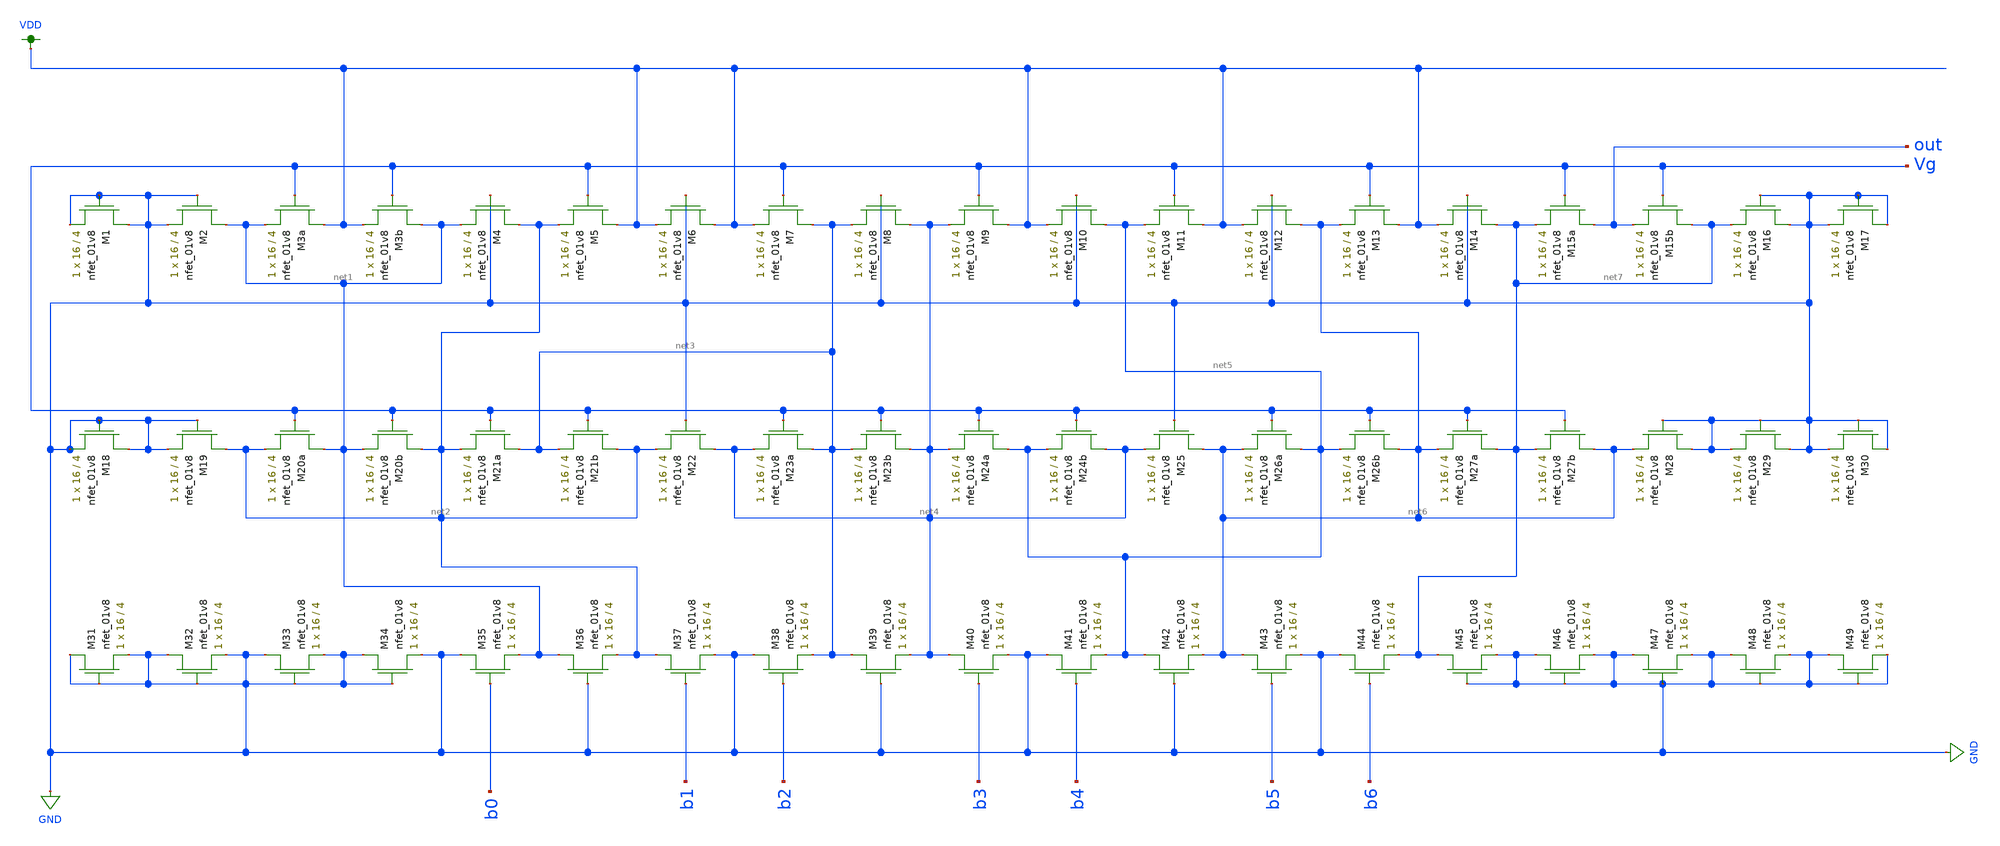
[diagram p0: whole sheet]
** sch_path: schematic/LDS/dac_7_bit_LDS.sch
**.subckt dac_7_bit_LDS
XM3a VDD Vg net1 GND sky130_fd_pr__nfet_01v8 L=4 W=16 nf=1 ad='int((nf+1)/2) * W/nf * 0.29' as='int((nf+2)/2) * W/nf * 0.29'
+ pd='2*int((nf+1)/2) * (W/nf + 0.29)' ps='2*int((nf+2)/2) * (W/nf + 0.29)' nrd='0.29 / W' nrs='0.29 / W'
+ sa=0 sb=0 sd=0 mult=1 m=1
XM3b net1 Vg VDD GND sky130_fd_pr__nfet_01v8 L=4 W=16 nf=1 ad='int((nf+1)/2) * W/nf * 0.29' as='int((nf+2)/2) * W/nf * 0.29'
+ pd='2*int((nf+1)/2) * (W/nf + 0.29)' ps='2*int((nf+2)/2) * (W/nf + 0.29)' nrd='0.29 / W' nrs='0.29 / W'
+ sa=0 sb=0 sd=0 mult=1 m=1
XM4 net2 GND net1 GND sky130_fd_pr__nfet_01v8 L=4 W=16 nf=1 ad='int((nf+1)/2) * W/nf * 0.29' as='int((nf+2)/2) * W/nf * 0.29'
+ pd='2*int((nf+1)/2) * (W/nf + 0.29)' ps='2*int((nf+2)/2) * (W/nf + 0.29)' nrd='0.29 / W' nrs='0.29 / W'
+ sa=0 sb=0 sd=0 mult=1 m=1
XM5 VDD Vg net2 GND sky130_fd_pr__nfet_01v8 L=4 W=16 nf=1 ad='int((nf+1)/2) * W/nf * 0.29' as='int((nf+2)/2) * W/nf * 0.29'
+ pd='2*int((nf+1)/2) * (W/nf + 0.29)' ps='2*int((nf+2)/2) * (W/nf + 0.29)' nrd='0.29 / W' nrs='0.29 / W'
+ sa=0 sb=0 sd=0 mult=1 m=1
XM6 VDD GND VDD GND sky130_fd_pr__nfet_01v8 L=4 W=16 nf=1 ad='int((nf+1)/2) * W/nf * 0.29' as='int((nf+2)/2) * W/nf * 0.29'
+ pd='2*int((nf+1)/2) * (W/nf + 0.29)' ps='2*int((nf+2)/2) * (W/nf + 0.29)' nrd='0.29 / W' nrs='0.29 / W'
+ sa=0 sb=0 sd=0 mult=1 m=1
XM7 net3 Vg VDD GND sky130_fd_pr__nfet_01v8 L=4 W=16 nf=1 ad='int((nf+1)/2) * W/nf * 0.29' as='int((nf+2)/2) * W/nf * 0.29'
+ pd='2*int((nf+1)/2) * (W/nf + 0.29)' ps='2*int((nf+2)/2) * (W/nf + 0.29)' nrd='0.29 / W' nrs='0.29 / W'
+ sa=0 sb=0 sd=0 mult=1 m=1
XM8 net4 GND net3 GND sky130_fd_pr__nfet_01v8 L=4 W=16 nf=1 ad='int((nf+1)/2) * W/nf * 0.29' as='int((nf+2)/2) * W/nf * 0.29'
+ pd='2*int((nf+1)/2) * (W/nf + 0.29)' ps='2*int((nf+2)/2) * (W/nf + 0.29)' nrd='0.29 / W' nrs='0.29 / W'
+ sa=0 sb=0 sd=0 mult=1 m=1
XM9 VDD Vg net4 GND sky130_fd_pr__nfet_01v8 L=4 W=16 nf=1 ad='int((nf+1)/2) * W/nf * 0.29' as='int((nf+2)/2) * W/nf * 0.29'
+ pd='2*int((nf+1)/2) * (W/nf + 0.29)' ps='2*int((nf+2)/2) * (W/nf + 0.29)' nrd='0.29 / W' nrs='0.29 / W'
+ sa=0 sb=0 sd=0 mult=1 m=1
XM10 net5 GND VDD GND sky130_fd_pr__nfet_01v8 L=4 W=16 nf=1 ad='int((nf+1)/2) * W/nf * 0.29' as='int((nf+2)/2) * W/nf * 0.29'
+ pd='2*int((nf+1)/2) * (W/nf + 0.29)' ps='2*int((nf+2)/2) * (W/nf + 0.29)' nrd='0.29 / W' nrs='0.29 / W'
+ sa=0 sb=0 sd=0 mult=1 m=1
XM11 VDD Vg net5 GND sky130_fd_pr__nfet_01v8 L=4 W=16 nf=1 ad='int((nf+1)/2) * W/nf * 0.29' as='int((nf+2)/2) * W/nf * 0.29'
+ pd='2*int((nf+1)/2) * (W/nf + 0.29)' ps='2*int((nf+2)/2) * (W/nf + 0.29)' nrd='0.29 / W' nrs='0.29 / W'
+ sa=0 sb=0 sd=0 mult=1 m=1
XM12 net6 GND VDD GND sky130_fd_pr__nfet_01v8 L=4 W=16 nf=1 ad='int((nf+1)/2) * W/nf * 0.29' as='int((nf+2)/2) * W/nf * 0.29'
+ pd='2*int((nf+1)/2) * (W/nf + 0.29)' ps='2*int((nf+2)/2) * (W/nf + 0.29)' nrd='0.29 / W' nrs='0.29 / W'
+ sa=0 sb=0 sd=0 mult=1 m=1
XM13 VDD Vg net6 GND sky130_fd_pr__nfet_01v8 L=4 W=16 nf=1 ad='int((nf+1)/2) * W/nf * 0.29' as='int((nf+2)/2) * W/nf * 0.29'
+ pd='2*int((nf+1)/2) * (W/nf + 0.29)' ps='2*int((nf+2)/2) * (W/nf + 0.29)' nrd='0.29 / W' nrs='0.29 / W'
+ sa=0 sb=0 sd=0 mult=1 m=1
XM14 net7 GND VDD GND sky130_fd_pr__nfet_01v8 L=4 W=16 nf=1 ad='int((nf+1)/2) * W/nf * 0.29' as='int((nf+2)/2) * W/nf * 0.29'
+ pd='2*int((nf+1)/2) * (W/nf + 0.29)' ps='2*int((nf+2)/2) * (W/nf + 0.29)' nrd='0.29 / W' nrs='0.29 / W'
+ sa=0 sb=0 sd=0 mult=1 m=1
XM15a out Vg net7 GND sky130_fd_pr__nfet_01v8 L=4 W=16 nf=1 ad='int((nf+1)/2) * W/nf * 0.29' as='int((nf+2)/2) * W/nf * 0.29'
+ pd='2*int((nf+1)/2) * (W/nf + 0.29)' ps='2*int((nf+2)/2) * (W/nf + 0.29)' nrd='0.29 / W' nrs='0.29 / W'
+ sa=0 sb=0 sd=0 mult=1 m=1
XM15b net7 Vg out GND sky130_fd_pr__nfet_01v8 L=4 W=16 nf=1 ad='int((nf+1)/2) * W/nf * 0.29' as='int((nf+2)/2) * W/nf * 0.29'
+ pd='2*int((nf+1)/2) * (W/nf + 0.29)' ps='2*int((nf+2)/2) * (W/nf + 0.29)' nrd='0.29 / W' nrs='0.29 / W'
+ sa=0 sb=0 sd=0 mult=1 m=1
XM20a net1 Vg net2 GND sky130_fd_pr__nfet_01v8 L=4 W=16 nf=1 ad='int((nf+1)/2) * W/nf * 0.29' as='int((nf+2)/2) * W/nf * 0.29'
+ pd='2*int((nf+1)/2) * (W/nf + 0.29)' ps='2*int((nf+2)/2) * (W/nf + 0.29)' nrd='0.29 / W' nrs='0.29 / W'
+ sa=0 sb=0 sd=0 mult=1 m=1
XM20b net2 Vg net1 GND sky130_fd_pr__nfet_01v8 L=4 W=16 nf=1 ad='int((nf+1)/2) * W/nf * 0.29' as='int((nf+2)/2) * W/nf * 0.29'
+ pd='2*int((nf+1)/2) * (W/nf + 0.29)' ps='2*int((nf+2)/2) * (W/nf + 0.29)' nrd='0.29 / W' nrs='0.29 / W'
+ sa=0 sb=0 sd=0 mult=1 m=1
XM21a net3 Vg net2 GND sky130_fd_pr__nfet_01v8 L=4 W=16 nf=1 ad='int((nf+1)/2) * W/nf * 0.29' as='int((nf+2)/2) * W/nf * 0.29'
+ pd='2*int((nf+1)/2) * (W/nf + 0.29)' ps='2*int((nf+2)/2) * (W/nf + 0.29)' nrd='0.29 / W' nrs='0.29 / W'
+ sa=0 sb=0 sd=0 mult=1 m=1
XM21b net2 Vg net3 GND sky130_fd_pr__nfet_01v8 L=4 W=16 nf=1 ad='int((nf+1)/2) * W/nf * 0.29' as='int((nf+2)/2) * W/nf * 0.29'
+ pd='2*int((nf+1)/2) * (W/nf + 0.29)' ps='2*int((nf+2)/2) * (W/nf + 0.29)' nrd='0.29 / W' nrs='0.29 / W'
+ sa=0 sb=0 sd=0 mult=1 m=1
XM22 net4 GND net2 GND sky130_fd_pr__nfet_01v8 L=4 W=16 nf=1 ad='int((nf+1)/2) * W/nf * 0.29' as='int((nf+2)/2) * W/nf * 0.29'
+ pd='2*int((nf+1)/2) * (W/nf + 0.29)' ps='2*int((nf+2)/2) * (W/nf + 0.29)' nrd='0.29 / W' nrs='0.29 / W'
+ sa=0 sb=0 sd=0 mult=1 m=1
XM23a net3 Vg net4 GND sky130_fd_pr__nfet_01v8 L=4 W=16 nf=1 ad='int((nf+1)/2) * W/nf * 0.29' as='int((nf+2)/2) * W/nf * 0.29'
+ pd='2*int((nf+1)/2) * (W/nf + 0.29)' ps='2*int((nf+2)/2) * (W/nf + 0.29)' nrd='0.29 / W' nrs='0.29 / W'
+ sa=0 sb=0 sd=0 mult=1 m=1
XM23b net4 Vg net3 GND sky130_fd_pr__nfet_01v8 L=4 W=16 nf=1 ad='int((nf+1)/2) * W/nf * 0.29' as='int((nf+2)/2) * W/nf * 0.29'
+ pd='2*int((nf+1)/2) * (W/nf + 0.29)' ps='2*int((nf+2)/2) * (W/nf + 0.29)' nrd='0.29 / W' nrs='0.29 / W'
+ sa=0 sb=0 sd=0 mult=1 m=1
XM24a net5 Vg net4 GND sky130_fd_pr__nfet_01v8 L=4 W=16 nf=1 ad='int((nf+1)/2) * W/nf * 0.29' as='int((nf+2)/2) * W/nf * 0.29'
+ pd='2*int((nf+1)/2) * (W/nf + 0.29)' ps='2*int((nf+2)/2) * (W/nf + 0.29)' nrd='0.29 / W' nrs='0.29 / W'
+ sa=0 sb=0 sd=0 mult=1 m=1
XM24b net4 Vg net5 GND sky130_fd_pr__nfet_01v8 L=4 W=16 nf=1 ad='int((nf+1)/2) * W/nf * 0.29' as='int((nf+2)/2) * W/nf * 0.29'
+ pd='2*int((nf+1)/2) * (W/nf + 0.29)' ps='2*int((nf+2)/2) * (W/nf + 0.29)' nrd='0.29 / W' nrs='0.29 / W'
+ sa=0 sb=0 sd=0 mult=1 m=1
XM25 net6 GND net4 GND sky130_fd_pr__nfet_01v8 L=4 W=16 nf=1 ad='int((nf+1)/2) * W/nf * 0.29' as='int((nf+2)/2) * W/nf * 0.29'
+ pd='2*int((nf+1)/2) * (W/nf + 0.29)' ps='2*int((nf+2)/2) * (W/nf + 0.29)' nrd='0.29 / W' nrs='0.29 / W'
+ sa=0 sb=0 sd=0 mult=1 m=1
XM26a net5 Vg net6 GND sky130_fd_pr__nfet_01v8 L=4 W=16 nf=1 ad='int((nf+1)/2) * W/nf * 0.29' as='int((nf+2)/2) * W/nf * 0.29'
+ pd='2*int((nf+1)/2) * (W/nf + 0.29)' ps='2*int((nf+2)/2) * (W/nf + 0.29)' nrd='0.29 / W' nrs='0.29 / W'
+ sa=0 sb=0 sd=0 mult=1 m=1
XM26b net6 Vg net5 GND sky130_fd_pr__nfet_01v8 L=4 W=16 nf=1 ad='int((nf+1)/2) * W/nf * 0.29' as='int((nf+2)/2) * W/nf * 0.29'
+ pd='2*int((nf+1)/2) * (W/nf + 0.29)' ps='2*int((nf+2)/2) * (W/nf + 0.29)' nrd='0.29 / W' nrs='0.29 / W'
+ sa=0 sb=0 sd=0 mult=1 m=1
XM27a net7 Vg net6 GND sky130_fd_pr__nfet_01v8 L=4 W=16 nf=1 ad='int((nf+1)/2) * W/nf * 0.29' as='int((nf+2)/2) * W/nf * 0.29'
+ pd='2*int((nf+1)/2) * (W/nf + 0.29)' ps='2*int((nf+2)/2) * (W/nf + 0.29)' nrd='0.29 / W' nrs='0.29 / W'
+ sa=0 sb=0 sd=0 mult=1 m=1
XM27b net6 Vg net7 GND sky130_fd_pr__nfet_01v8 L=4 W=16 nf=1 ad='int((nf+1)/2) * W/nf * 0.29' as='int((nf+2)/2) * W/nf * 0.29'
+ pd='2*int((nf+1)/2) * (W/nf + 0.29)' ps='2*int((nf+2)/2) * (W/nf + 0.29)' nrd='0.29 / W' nrs='0.29 / W'
+ sa=0 sb=0 sd=0 mult=1 m=1
XM35 GND b0 net1 GND sky130_fd_pr__nfet_01v8 L=4 W=16 nf=1 ad='int((nf+1)/2) * W/nf * 0.29' as='int((nf+2)/2) * W/nf * 0.29'
+ pd='2*int((nf+1)/2) * (W/nf + 0.29)' ps='2*int((nf+2)/2) * (W/nf + 0.29)' nrd='0.29 / W' nrs='0.29 / W'
+ sa=0 sb=0 sd=0 mult=1 m=1
XM36 net1 GND net2 GND sky130_fd_pr__nfet_01v8 L=4 W=16 nf=1 ad='int((nf+1)/2) * W/nf * 0.29' as='int((nf+2)/2) * W/nf * 0.29'
+ pd='2*int((nf+1)/2) * (W/nf + 0.29)' ps='2*int((nf+2)/2) * (W/nf + 0.29)' nrd='0.29 / W' nrs='0.29 / W'
+ sa=0 sb=0 sd=0 mult=1 m=1
XM37 net2 b1 GND GND sky130_fd_pr__nfet_01v8 L=4 W=16 nf=1 ad='int((nf+1)/2) * W/nf * 0.29' as='int((nf+2)/2) * W/nf * 0.29'
+ pd='2*int((nf+1)/2) * (W/nf + 0.29)' ps='2*int((nf+2)/2) * (W/nf + 0.29)' nrd='0.29 / W' nrs='0.29 / W'
+ sa=0 sb=0 sd=0 mult=1 m=1
XM38 GND b2 net3 GND sky130_fd_pr__nfet_01v8 L=4 W=16 nf=1 ad='int((nf+1)/2) * W/nf * 0.29' as='int((nf+2)/2) * W/nf * 0.29'
+ pd='2*int((nf+1)/2) * (W/nf + 0.29)' ps='2*int((nf+2)/2) * (W/nf + 0.29)' nrd='0.29 / W' nrs='0.29 / W'
+ sa=0 sb=0 sd=0 mult=1 m=1
XM39 net3 GND net4 GND sky130_fd_pr__nfet_01v8 L=4 W=16 nf=1 ad='int((nf+1)/2) * W/nf * 0.29' as='int((nf+2)/2) * W/nf * 0.29'
+ pd='2*int((nf+1)/2) * (W/nf + 0.29)' ps='2*int((nf+2)/2) * (W/nf + 0.29)' nrd='0.29 / W' nrs='0.29 / W'
+ sa=0 sb=0 sd=0 mult=1 m=1
XM40 net4 b3 GND GND sky130_fd_pr__nfet_01v8 L=4 W=16 nf=1 ad='int((nf+1)/2) * W/nf * 0.29' as='int((nf+2)/2) * W/nf * 0.29'
+ pd='2*int((nf+1)/2) * (W/nf + 0.29)' ps='2*int((nf+2)/2) * (W/nf + 0.29)' nrd='0.29 / W' nrs='0.29 / W'
+ sa=0 sb=0 sd=0 mult=1 m=1
XM41 GND b4 net5 GND sky130_fd_pr__nfet_01v8 L=4 W=16 nf=1 ad='int((nf+1)/2) * W/nf * 0.29' as='int((nf+2)/2) * W/nf * 0.29'
+ pd='2*int((nf+1)/2) * (W/nf + 0.29)' ps='2*int((nf+2)/2) * (W/nf + 0.29)' nrd='0.29 / W' nrs='0.29 / W'
+ sa=0 sb=0 sd=0 mult=1 m=1
XM42 net5 GND net6 GND sky130_fd_pr__nfet_01v8 L=4 W=16 nf=1 ad='int((nf+1)/2) * W/nf * 0.29' as='int((nf+2)/2) * W/nf * 0.29'
+ pd='2*int((nf+1)/2) * (W/nf + 0.29)' ps='2*int((nf+2)/2) * (W/nf + 0.29)' nrd='0.29 / W' nrs='0.29 / W'
+ sa=0 sb=0 sd=0 mult=1 m=1
XM43 net6 b5 GND GND sky130_fd_pr__nfet_01v8 L=4 W=16 nf=1 ad='int((nf+1)/2) * W/nf * 0.29' as='int((nf+2)/2) * W/nf * 0.29'
+ pd='2*int((nf+1)/2) * (W/nf + 0.29)' ps='2*int((nf+2)/2) * (W/nf + 0.29)' nrd='0.29 / W' nrs='0.29 / W'
+ sa=0 sb=0 sd=0 mult=1 m=1
XM44 GND b6 net7 GND sky130_fd_pr__nfet_01v8 L=4 W=16 nf=1 ad='int((nf+1)/2) * W/nf * 0.29' as='int((nf+2)/2) * W/nf * 0.29'
+ pd='2*int((nf+1)/2) * (W/nf + 0.29)' ps='2*int((nf+2)/2) * (W/nf + 0.29)' nrd='0.29 / W' nrs='0.29 / W'
+ sa=0 sb=0 sd=0 mult=1 m=1
XM16 GND GND net7 GND sky130_fd_pr__nfet_01v8 L=4 W=16 nf=1 ad='int((nf+1)/2) * W/nf * 0.29' as='int((nf+2)/2) * W/nf * 0.29'
+ pd='2*int((nf+1)/2) * (W/nf + 0.29)' ps='2*int((nf+2)/2) * (W/nf + 0.29)' nrd='0.29 / W' nrs='0.29 / W'
+ sa=0 sb=0 sd=0 mult=1 m=1
XM17 GND GND GND GND sky130_fd_pr__nfet_01v8 L=4 W=16 nf=1 ad='int((nf+1)/2) * W/nf * 0.29' as='int((nf+2)/2) * W/nf * 0.29'
+ pd='2*int((nf+1)/2) * (W/nf + 0.29)' ps='2*int((nf+2)/2) * (W/nf + 0.29)' nrd='0.29 / W' nrs='0.29 / W'
+ sa=0 sb=0 sd=0 mult=1 m=1
XM2 net1 GND GND GND sky130_fd_pr__nfet_01v8 L=4 W=16 nf=1 ad='int((nf+1)/2) * W/nf * 0.29' as='int((nf+2)/2) * W/nf * 0.29'
+ pd='2*int((nf+1)/2) * (W/nf + 0.29)' ps='2*int((nf+2)/2) * (W/nf + 0.29)' nrd='0.29 / W' nrs='0.29 / W'
+ sa=0 sb=0 sd=0 mult=1 m=1
XM1 GND GND GND GND sky130_fd_pr__nfet_01v8 L=4 W=16 nf=1 ad='int((nf+1)/2) * W/nf * 0.29' as='int((nf+2)/2) * W/nf * 0.29'
+ pd='2*int((nf+1)/2) * (W/nf + 0.29)' ps='2*int((nf+2)/2) * (W/nf + 0.29)' nrd='0.29 / W' nrs='0.29 / W'
+ sa=0 sb=0 sd=0 mult=1 m=1
XM19 net2 GND GND GND sky130_fd_pr__nfet_01v8 L=4 W=16 nf=1 ad='int((nf+1)/2) * W/nf * 0.29' as='int((nf+2)/2) * W/nf * 0.29'
+ pd='2*int((nf+1)/2) * (W/nf + 0.29)' ps='2*int((nf+2)/2) * (W/nf + 0.29)' nrd='0.29 / W' nrs='0.29 / W'
+ sa=0 sb=0 sd=0 mult=1 m=1
XM18 GND GND GND GND sky130_fd_pr__nfet_01v8 L=4 W=16 nf=1 ad='int((nf+1)/2) * W/nf * 0.29' as='int((nf+2)/2) * W/nf * 0.29'
+ pd='2*int((nf+1)/2) * (W/nf + 0.29)' ps='2*int((nf+2)/2) * (W/nf + 0.29)' nrd='0.29 / W' nrs='0.29 / W'
+ sa=0 sb=0 sd=0 mult=1 m=1
XM28 GND GND net6 GND sky130_fd_pr__nfet_01v8 L=4 W=16 nf=1 ad='int((nf+1)/2) * W/nf * 0.29' as='int((nf+2)/2) * W/nf * 0.29'
+ pd='2*int((nf+1)/2) * (W/nf + 0.29)' ps='2*int((nf+2)/2) * (W/nf + 0.29)' nrd='0.29 / W' nrs='0.29 / W'
+ sa=0 sb=0 sd=0 mult=1 m=1
XM29 GND GND GND GND sky130_fd_pr__nfet_01v8 L=4 W=16 nf=1 ad='int((nf+1)/2) * W/nf * 0.29' as='int((nf+2)/2) * W/nf * 0.29'
+ pd='2*int((nf+1)/2) * (W/nf + 0.29)' ps='2*int((nf+2)/2) * (W/nf + 0.29)' nrd='0.29 / W' nrs='0.29 / W'
+ sa=0 sb=0 sd=0 mult=1 m=1
XM30 GND GND GND GND sky130_fd_pr__nfet_01v8 L=4 W=16 nf=1 ad='int((nf+1)/2) * W/nf * 0.29' as='int((nf+2)/2) * W/nf * 0.29'
+ pd='2*int((nf+1)/2) * (W/nf + 0.29)' ps='2*int((nf+2)/2) * (W/nf + 0.29)' nrd='0.29 / W' nrs='0.29 / W'
+ sa=0 sb=0 sd=0 mult=1 m=1
XM45 net7 GND GND GND sky130_fd_pr__nfet_01v8 L=4 W=16 nf=1 ad='int((nf+1)/2) * W/nf * 0.29' as='int((nf+2)/2) * W/nf * 0.29'
+ pd='2*int((nf+1)/2) * (W/nf + 0.29)' ps='2*int((nf+2)/2) * (W/nf + 0.29)' nrd='0.29 / W' nrs='0.29 / W'
+ sa=0 sb=0 sd=0 mult=1 m=1
XM46 GND GND GND GND sky130_fd_pr__nfet_01v8 L=4 W=16 nf=1 ad='int((nf+1)/2) * W/nf * 0.29' as='int((nf+2)/2) * W/nf * 0.29'
+ pd='2*int((nf+1)/2) * (W/nf + 0.29)' ps='2*int((nf+2)/2) * (W/nf + 0.29)' nrd='0.29 / W' nrs='0.29 / W'
+ sa=0 sb=0 sd=0 mult=1 m=1
XM47 GND GND GND GND sky130_fd_pr__nfet_01v8 L=4 W=16 nf=1 ad='int((nf+1)/2) * W/nf * 0.29' as='int((nf+2)/2) * W/nf * 0.29'
+ pd='2*int((nf+1)/2) * (W/nf + 0.29)' ps='2*int((nf+2)/2) * (W/nf + 0.29)' nrd='0.29 / W' nrs='0.29 / W'
+ sa=0 sb=0 sd=0 mult=1 m=1
XM48 GND GND GND GND sky130_fd_pr__nfet_01v8 L=4 W=16 nf=1 ad='int((nf+1)/2) * W/nf * 0.29' as='int((nf+2)/2) * W/nf * 0.29'
+ pd='2*int((nf+1)/2) * (W/nf + 0.29)' ps='2*int((nf+2)/2) * (W/nf + 0.29)' nrd='0.29 / W' nrs='0.29 / W'
+ sa=0 sb=0 sd=0 mult=1 m=1
XM49 GND GND GND GND sky130_fd_pr__nfet_01v8 L=4 W=16 nf=1 ad='int((nf+1)/2) * W/nf * 0.29' as='int((nf+2)/2) * W/nf * 0.29'
+ pd='2*int((nf+1)/2) * (W/nf + 0.29)' ps='2*int((nf+2)/2) * (W/nf + 0.29)' nrd='0.29 / W' nrs='0.29 / W'
+ sa=0 sb=0 sd=0 mult=1 m=1
XM34 GND GND GND GND sky130_fd_pr__nfet_01v8 L=4 W=16 nf=1 ad='int((nf+1)/2) * W/nf * 0.29' as='int((nf+2)/2) * W/nf * 0.29'
+ pd='2*int((nf+1)/2) * (W/nf + 0.29)' ps='2*int((nf+2)/2) * (W/nf + 0.29)' nrd='0.29 / W' nrs='0.29 / W'
+ sa=0 sb=0 sd=0 mult=1 m=1
XM33 GND GND GND GND sky130_fd_pr__nfet_01v8 L=4 W=16 nf=1 ad='int((nf+1)/2) * W/nf * 0.29' as='int((nf+2)/2) * W/nf * 0.29'
+ pd='2*int((nf+1)/2) * (W/nf + 0.29)' ps='2*int((nf+2)/2) * (W/nf + 0.29)' nrd='0.29 / W' nrs='0.29 / W'
+ sa=0 sb=0 sd=0 mult=1 m=1
XM32 GND GND GND GND sky130_fd_pr__nfet_01v8 L=4 W=16 nf=1 ad='int((nf+1)/2) * W/nf * 0.29' as='int((nf+2)/2) * W/nf * 0.29'
+ pd='2*int((nf+1)/2) * (W/nf + 0.29)' ps='2*int((nf+2)/2) * (W/nf + 0.29)' nrd='0.29 / W' nrs='0.29 / W'
+ sa=0 sb=0 sd=0 mult=1 m=1
XM31 GND GND GND GND sky130_fd_pr__nfet_01v8 L=4 W=16 nf=1 ad='int((nf+1)/2) * W/nf * 0.29' as='int((nf+2)/2) * W/nf * 0.29'
+ pd='2*int((nf+1)/2) * (W/nf + 0.29)' ps='2*int((nf+2)/2) * (W/nf + 0.29)' nrd='0.29 / W' nrs='0.29 / W'
+ sa=0 sb=0 sd=0 mult=1 m=1
**.ends
.GLOBAL GND
.GLOBAL VDD
.end
